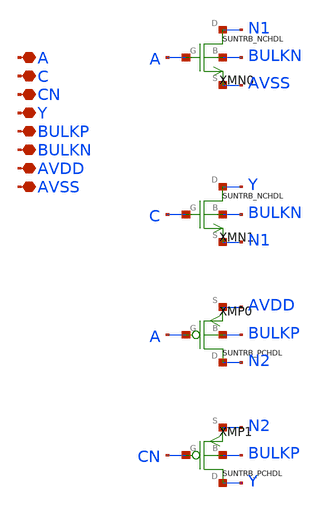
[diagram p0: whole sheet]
** sch_path: ip/sun_trb_sky130nm/design/SUN_TRB_SKY130NM/SUNTRB_IVTRIX1_CV.sch
**.subckt SUNTRB_IVTRIX1_CV A C CN Y BULKP BULKN AVDD AVSS
*.iopin A
*.iopin C
*.iopin CN
*.iopin Y
*.iopin BULKP
*.iopin BULKN
*.iopin AVDD
*.iopin AVSS
XMN0 N1 A AVSS BULKN SUNTRB_NCHDL xoffset=0 yoffset=0 angle=0
XMN1 Y C N1 BULKN SUNTRB_NCHDL xoffset=0 yoffset=0 angle=0
XMP0 N2 A AVDD BULKP SUNTRB_PCHDL xoffset=0 yoffset=0 angle=0
XMP1 Y CN N2 BULKP SUNTRB_PCHDL xoffset=0 yoffset=0 angle=0
**.ends
.end
